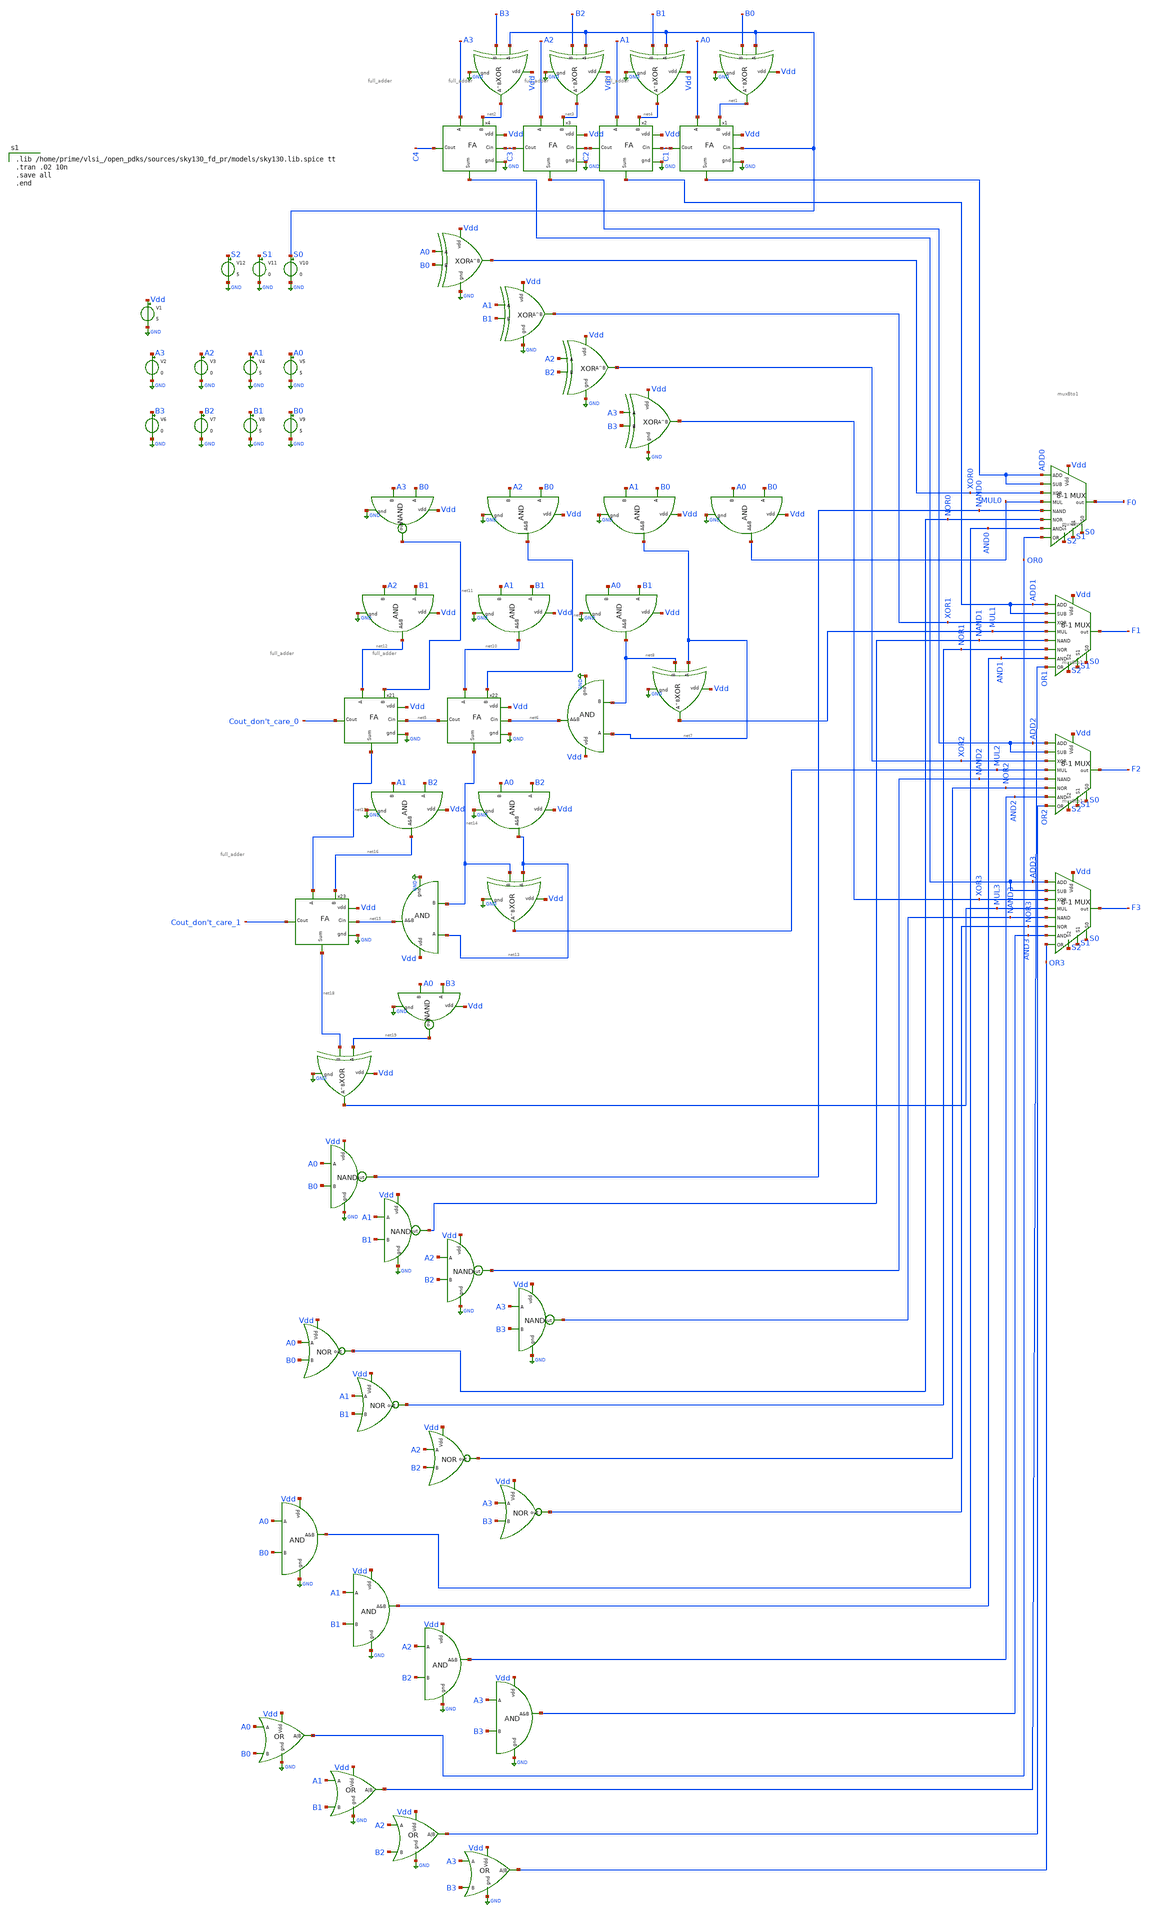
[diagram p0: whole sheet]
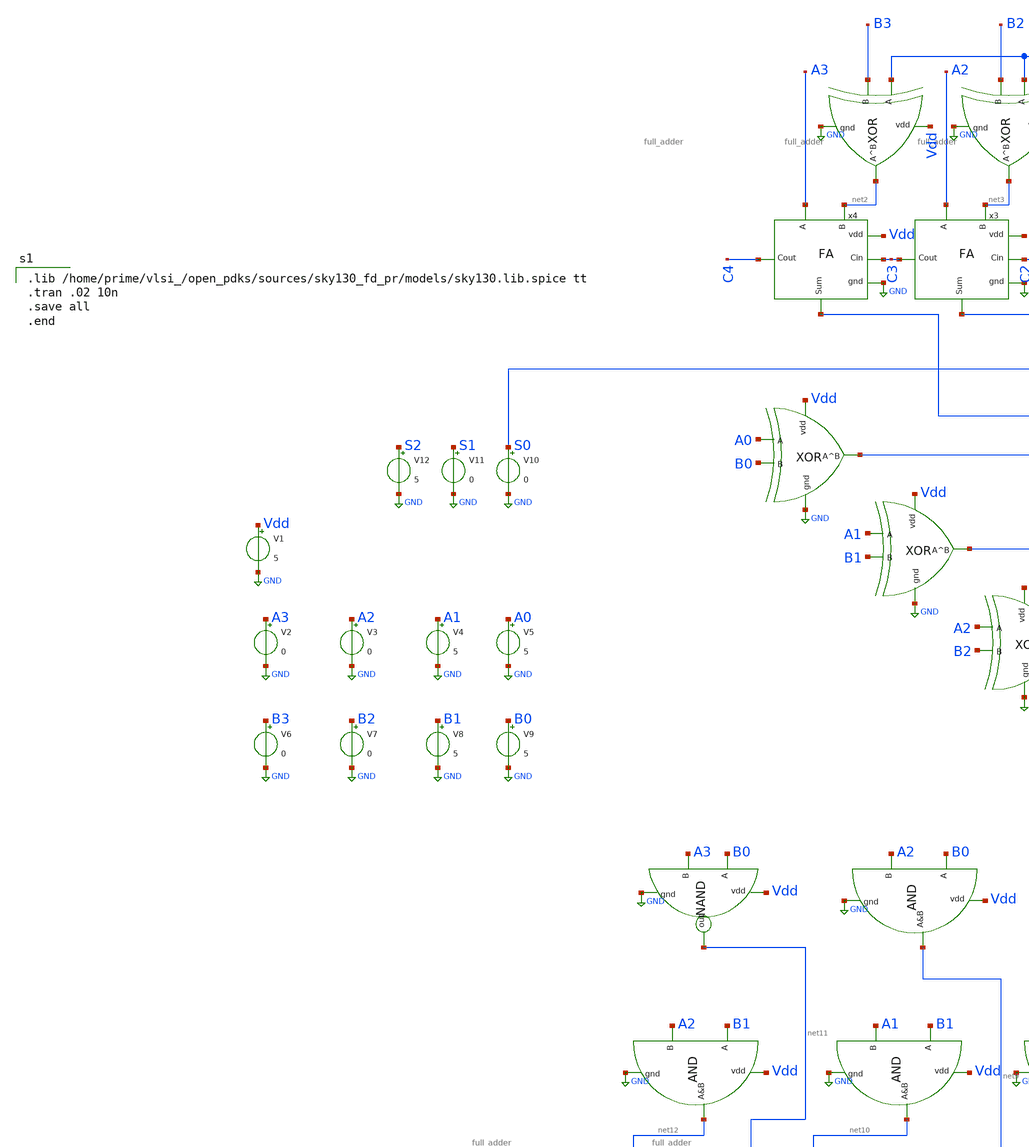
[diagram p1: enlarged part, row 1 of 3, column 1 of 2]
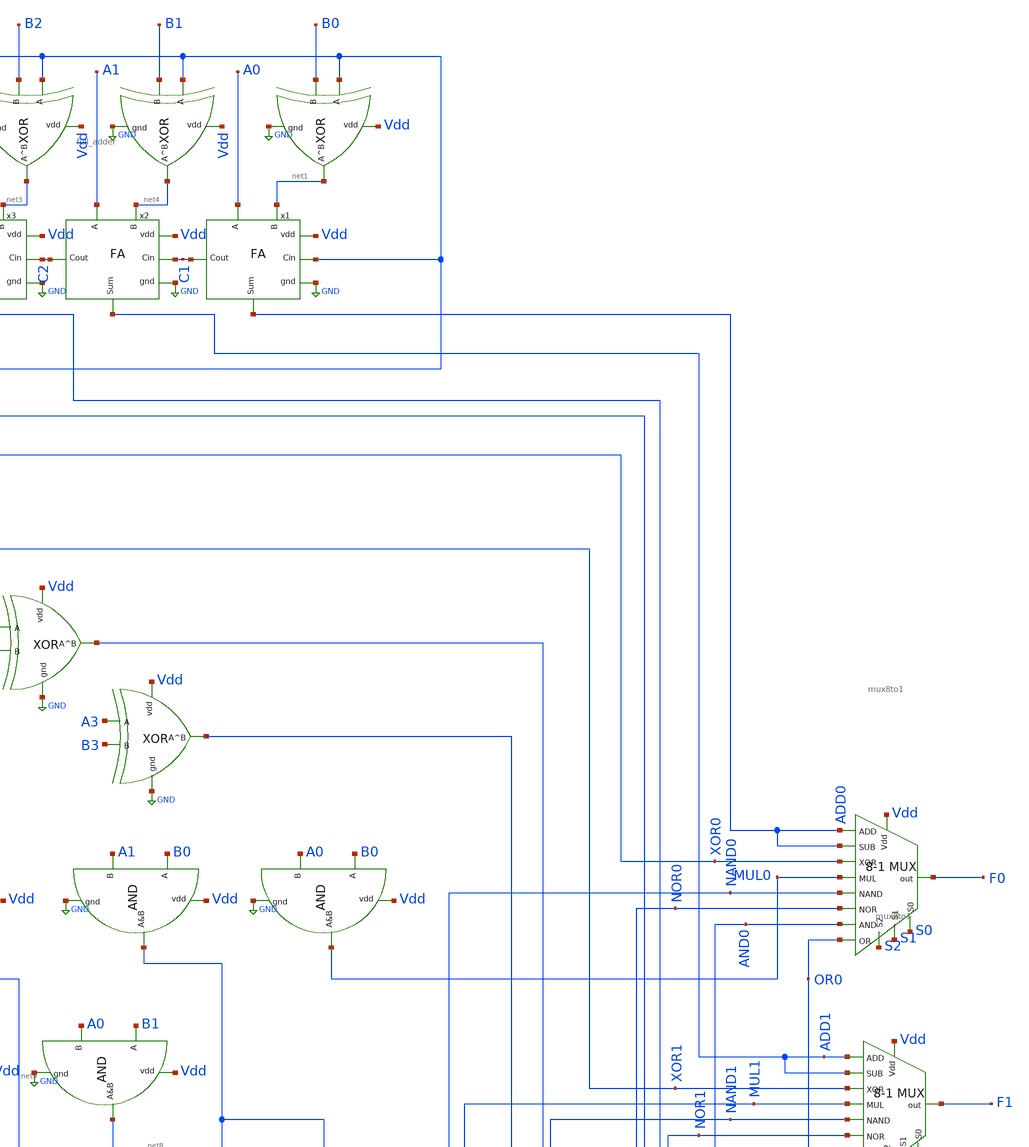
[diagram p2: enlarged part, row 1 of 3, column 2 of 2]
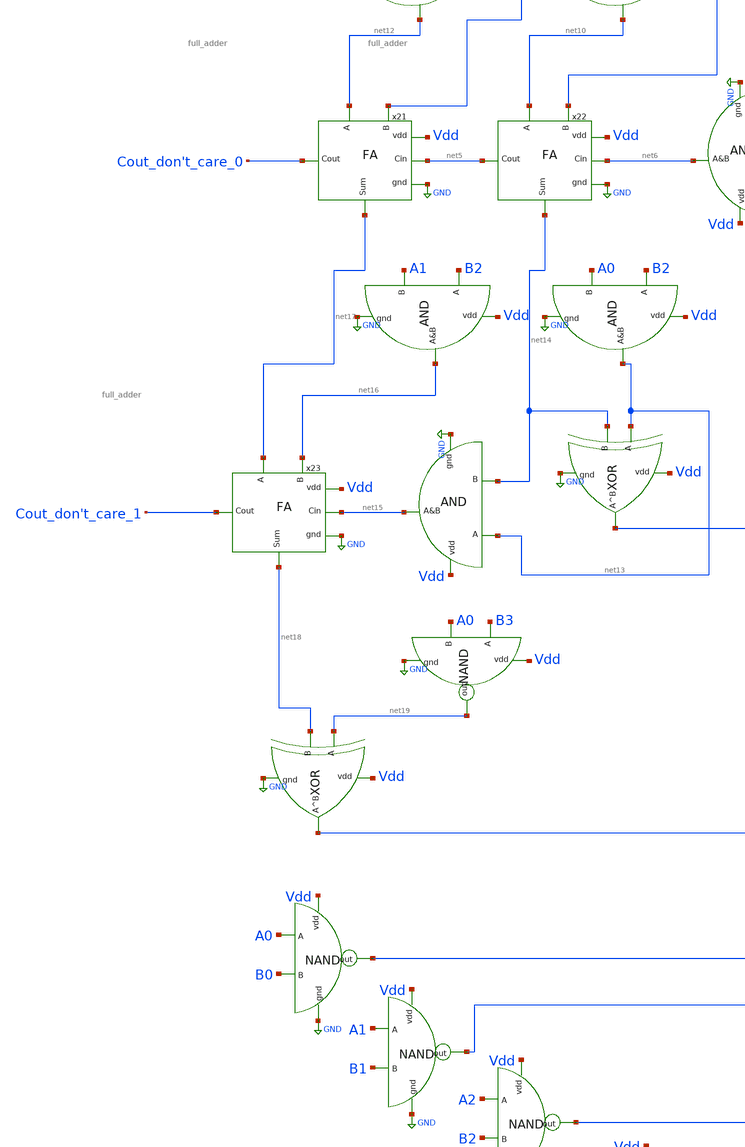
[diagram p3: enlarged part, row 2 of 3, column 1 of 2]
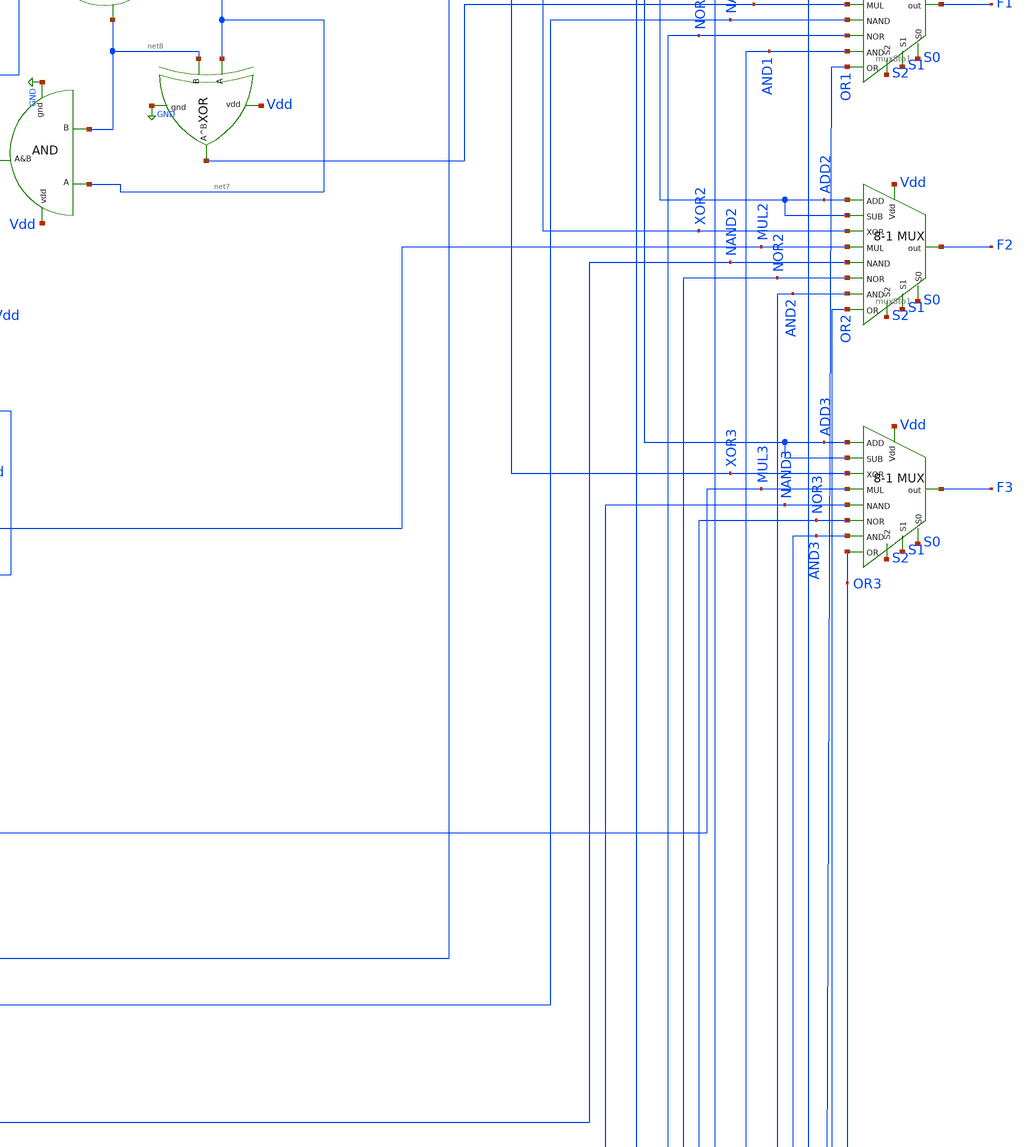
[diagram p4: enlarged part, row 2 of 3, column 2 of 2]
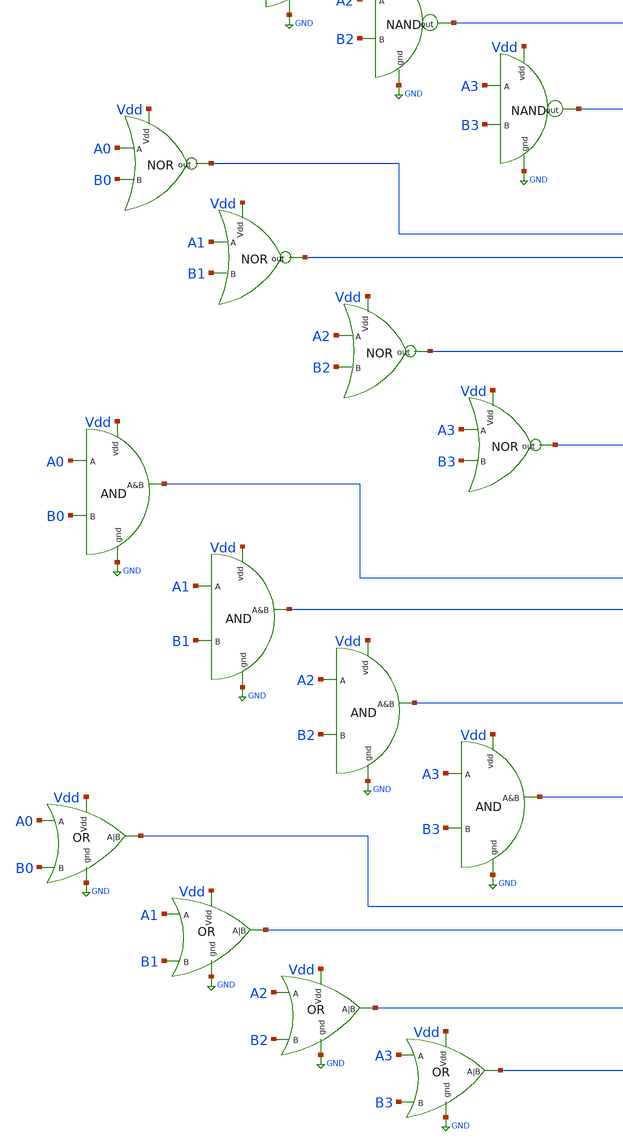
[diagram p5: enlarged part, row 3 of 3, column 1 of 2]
** sch_path: schematics/alu.sch
**.subckt alu
x1 ADD0 C1 S0 Vdd GND A0 net1 full_adder
x2 ADD1 C2 C1 Vdd GND A1 net4 full_adder
x3 ADD2 C3 C2 Vdd GND A2 net3 full_adder
x4 ADD3 C4 C3 Vdd GND A3 net2 full_adder
x5 Vdd GND net1 S0 B0 xor
x6 Vdd GND net4 S0 B1 xor
x7 Vdd GND net3 S0 B2 xor
x8 Vdd GND net2 S0 B3 xor
V1 Vdd GND 5
V2 A3 GND 0
V3 A2 GND 0
V4 A1 GND 5
V5 A0 GND 5
V6 B3 GND 0
V7 B2 GND 0
V8 B1 GND 5
V9 B0 GND 5
V10 S0 GND 0
x9 Vdd GND XOR0 A0 B0 xor
x10 A0 B0 AND0 Vdd GND and
x11 Vdd GND OR0 A0 B0 or
x12 Vdd GND XOR1 A1 B1 xor
x13 Vdd GND XOR2 A2 B2 xor
x14 A1 B1 AND1 Vdd GND and
x15 A2 B2 AND2 Vdd GND and
x16 Vdd GND XOR3 A3 B3 xor
x17 A3 B3 AND3 Vdd GND and
x18 Vdd GND OR1 A1 B1 or
x19 Vdd GND OR2 A2 B2 or
x20 Vdd GND OR3 A3 B3 or
x21 net17 Cout_don't_care_0 net5 Vdd GND net12 net11 full_adder
x22 net14 net5 net6 Vdd GND net10 net9 full_adder
x23 net18 Cout_don't_care_1 net15 Vdd GND net17 net16 full_adder
x24 Vdd GND MUL1 net7 net8 xor
x25 net7 net8 net6 Vdd GND and
x26 net11 Vdd B0 A3 GND NAND
x27 B0 A2 net9 Vdd GND and
x28 B0 A1 net7 Vdd GND and
x29 B0 A0 MUL0 Vdd GND and
x30 B1 A2 net12 Vdd GND and
x31 B1 A1 net10 Vdd GND and
x32 B1 A0 net8 Vdd GND and
x33 B2 A1 net16 Vdd GND and
x34 B2 A0 net13 Vdd GND and
x35 Vdd GND MUL2 net13 net14 xor
x36 net13 net14 net15 Vdd GND and
x37 Vdd GND MUL3 net19 net18 xor
x38 net19 Vdd B3 A0 GND NAND
V11 S1 GND 0
V12 S2 GND 5
x39 NAND0 Vdd A0 B0 GND NAND
x40 NAND1 Vdd A1 B1 GND NAND
x41 NAND2 Vdd A2 B2 GND NAND
x42 NAND3 Vdd A3 B3 GND NAND
x43 NOR0 Vdd A0 B0 nor
x44 NOR1 Vdd A1 B1 nor
x45 NOR2 Vdd A2 B2 nor
x46 NOR3 Vdd A3 B3 nor
x47 F0 ADD0 ADD0 XOR0 MUL0 Vdd NAND0 NOR0 AND0 OR0 S0 S1 S2 mux8to1
x48 F1 ADD1 ADD1 XOR1 MUL1 Vdd NAND1 NOR1 AND1 OR1 S0 S1 S2 mux8to1
x49 F2 ADD2 ADD2 XOR2 MUL2 Vdd NAND2 NOR2 AND2 OR2 S0 S1 S2 mux8to1
x50 F3 ADD3 ADD3 XOR3 MUL3 Vdd NAND3 NOR3 AND3 OR3 S0 S1 S2 mux8to1
**** begin user architecture code

.lib /home/prime/vlsi_/open_pdks/sources/sky130_fd_pr/models/sky130.lib.spice tt
.tran .02 10n
.save all
.end

**** end user architecture code
**.ends
.GLOBAL GND
.end
